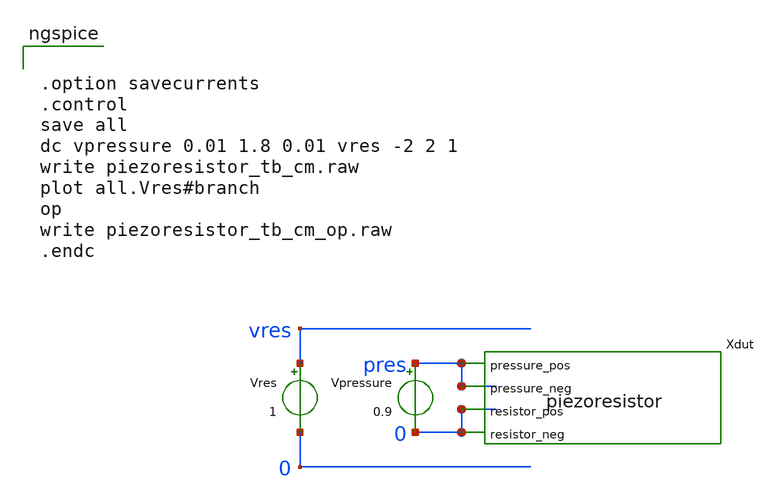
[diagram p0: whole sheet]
** sch_path: piezoresistor_tb_cm.sch
* Copyright 2020 Stefan Frederik Schippers
* Licensed under the Apache License, Version 2.0 (the "License");
* you may not use this file except in compliance with the License.
* You may obtain a copy of the License at
* https://www.apache.org/licenses/LICENSE-2.0
* Unless required by applicable law or agreed to in writing, software
* distributed under the License is distributed on an "AS IS" BASIS,
* WITHOUT WARRANTIES OR CONDITIONS OF ANY KIND, either express or implied.
* See the License for the specific language governing permissions and
* limitations under the License.
**.subckt piezoresistor_tb_cm
Xdut pres pres 0 0 piezoresistor
Vres vres 0 1
Vpressure pres 0 0.9
**** begin user architecture code


.option savecurrents
.control
save all
dc vpressure 0.01 1.8 0.01 vres -2 2 1
write piezoresistor_tb_cm.raw
plot all.Vres#branch
op
write piezoresistor_tb_cm_op.raw
.endc


**** end user architecture code
**.ends

* expanding   symbol:  piezoresistor.sym # of pins=4
** sym_path: piezoresistor.sym
** sch_path: piezoresistor.sch
.subckt piezoresistor pressure_pos pressure_neg resistor_pos resistor_neg
*.ipin pressure_pos
*.ipin pressure_neg
*.iopin resistor_pos
*.iopin resistor_neg
Broot sqrtp 0 V = sqrt(v(pressure_pos,pressure_neg))
Bres res 0 V = 106*(50/v(sqrtp)-1)*exp(-0.328*v(sqrtp))+15
Brvar resistor_pos resistor_neg I = V(resistor_pos,resistor_neg)/V(res)
.ends

.end
